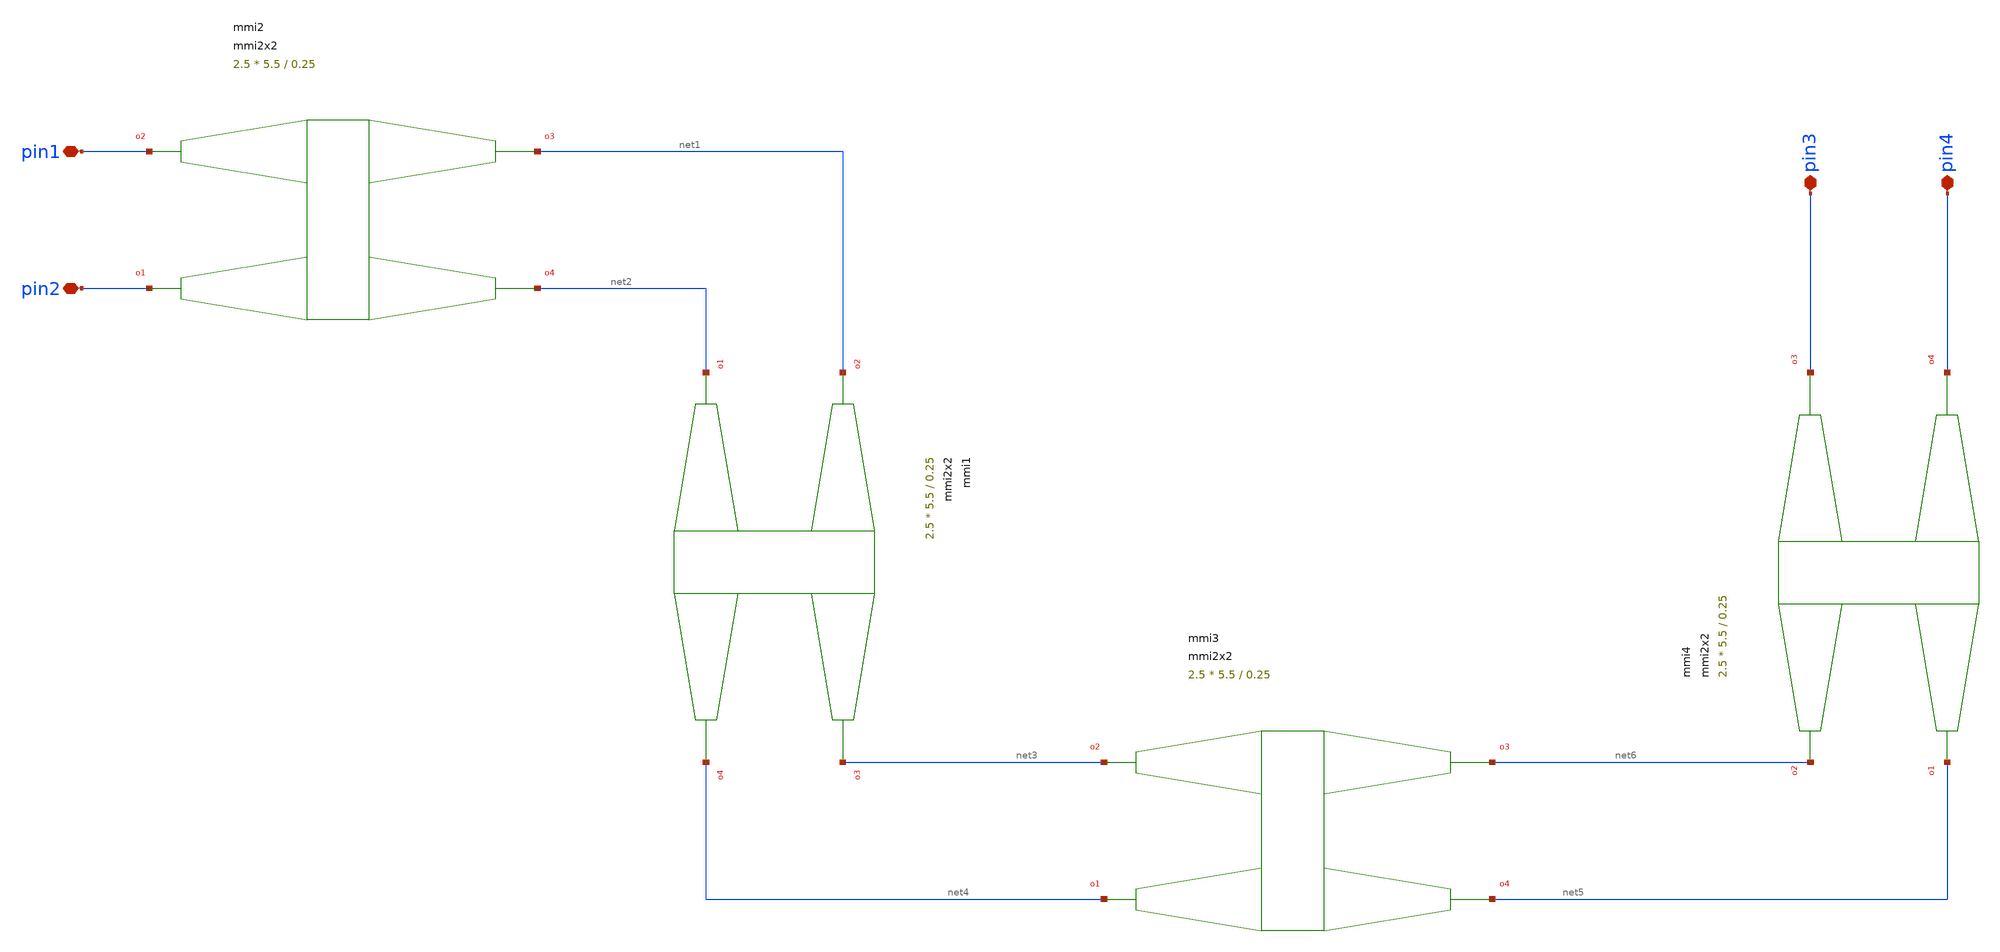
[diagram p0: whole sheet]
** sch_path: cells/xschem/tests/test_mmi2x2.sch
* SPDX-FileCopyrightText: 2023 Mabrains Company
* Licensed under the GNU GENERAL PUBLIC License, Version 3.0 (the "License");
* you may not use this file except in compliance with the License.
* GNU GENERAL PUBLIC LICENSE
* Version 3, 29 June 2007
* This program is free software: you can redistribute it and/or modify
* it under the terms of the GNU General Public License as published
* by the Free Software Foundation, either 3 of the License, or
* (at your option) any later version.
* This program is distributed in the hope that it will be useful,
* but WITHOUT ANY WARRANTY; without even the implied warranty of
* MERCHANTABILITY or FITNESS FOR A PARTICULAR PURPOSE.  See the
* GNU General Public License for more details.
* You should have received a copy of the GNU General Public License
* along with this program.  If not, see <https://www.gnu.org/licenses/>.
* SPDX-License-Identifier: GPL-3.0
**.subckt test_mmi2x2 pin1 pin2 pin3 pin4
*.iopin pin1
*.iopin pin2
*.iopin pin3
*.iopin pin4
Pmmi2 pin2 pin1 net1 net2 mmi2x2 width=0.5 width_taper=1 length_taper=10 length_mmi=5.5
+ width_mmi=2.5 gap_mmi=0.25
Pmmi1 net2 net1 net3 net4 mmi2x2 width=0.5 width_taper=1 length_taper=10 length_mmi=5.5
+ width_mmi=2.5 gap_mmi=0.25
Pmmi3 net4 net3 net6 net5 mmi2x2 width=0.5 width_taper=1 length_taper=10 length_mmi=5.5
+ width_mmi=2.5 gap_mmi=0.25
Pmmi4 net5 net6 pin3 pin4 mmi2x2 width=0.5 width_taper=1 length_taper=10 length_mmi=5.5
+ width_mmi=2.5 gap_mmi=0.25
**.ends
.end
